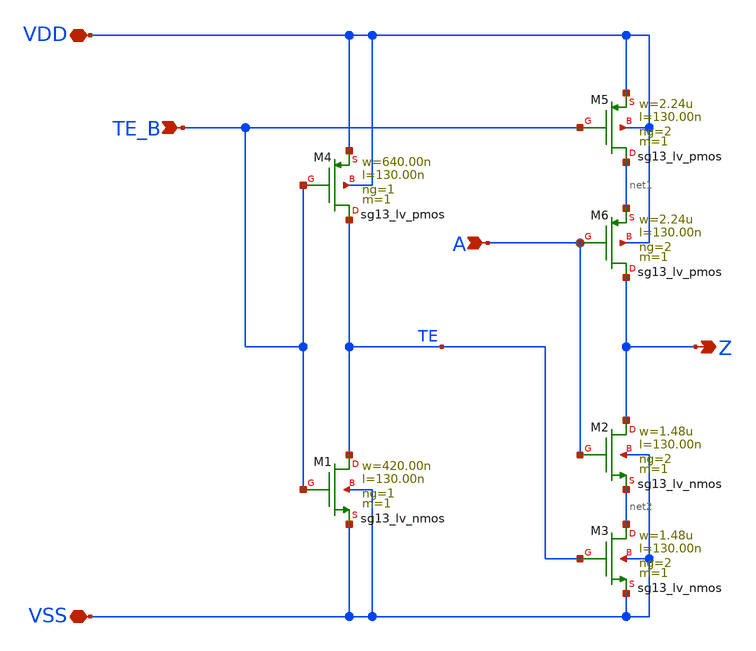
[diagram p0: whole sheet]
** sch_path: ihp-sg13g2/libs.tech/xschem/sg13g2_stdcells/sg13g2_einvn_2.sch
**.subckt sg13g2_einvn_2 TE_B A Z VDD VSS
*.ipin TE_B
*.ipin A
*.opin Z
*.iopin VDD
*.iopin VSS
XM1 TE TE_B VSS VSS sg13_lv_nmos w=420.00n l=130.00n ng=1 m=1 mm_ok=1
XM2 Z A net2 VSS sg13_lv_nmos w=1.48u l=130.00n ng=2 m=1 mm_ok=1
XM3 net2 TE VSS VSS sg13_lv_nmos w=1.48u l=130.00n ng=2 m=1 mm_ok=1
XM4 TE TE_B VDD VDD sg13_lv_pmos w=640.00n l=130.00n ng=1 m=1 mm_ok=1
XM5 net1 TE_B VDD VDD sg13_lv_pmos w=2.24u l=130.00n ng=2 m=1 mm_ok=1
XM6 Z A net1 VDD sg13_lv_pmos w=2.24u l=130.00n ng=2 m=1 mm_ok=1
**.ends
.end
